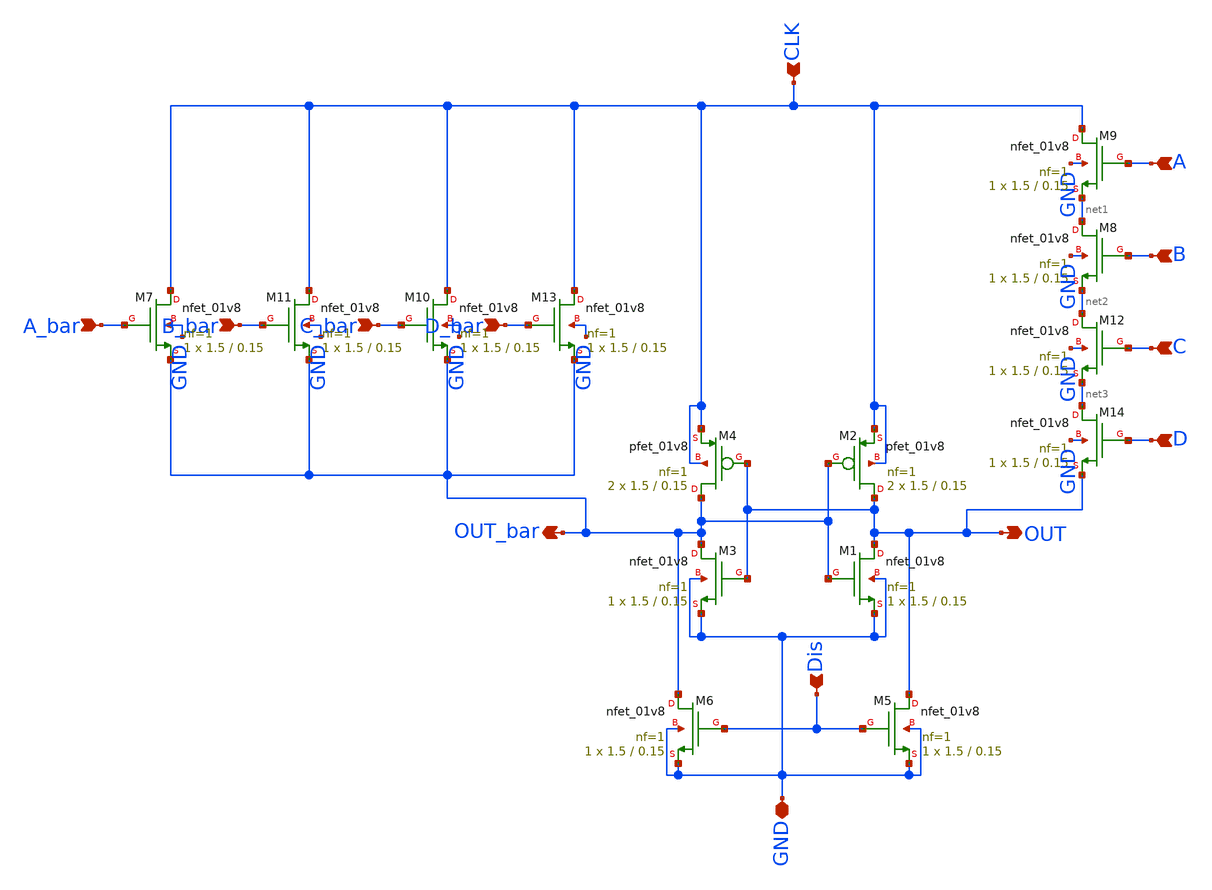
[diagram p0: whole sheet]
** sch_path: skywater_stuff/EESPFAL_4in_NAND.sch
**.subckt EESPFAL_4in_NAND A A_bar B B_bar C C_bar D D_bar OUT OUT_bar Dis GND CLK
*.ipin A
*.ipin A_bar
*.ipin B
*.ipin B_bar
*.ipin C
*.ipin C_bar
*.ipin D
*.ipin D_bar
*.opin OUT
*.opin OUT_bar
*.ipin Dis
*.iopin GND
*.ipin CLK
XM2 OUT OUT_bar CLK CLK sky130_fd_pr__pfet_01v8 L=0.15 W=1.5 nf=1 ad='int((nf+1)/2) * W/nf * 0.29' as='int((nf+2)/2) * W/nf * 0.29'
+ pd='2*int((nf+1)/2) * (W/nf + 0.29)' ps='2*int((nf+2)/2) * (W/nf + 0.29)' nrd='0.29 / W' nrs='0.29 / W'
+ sa=0 sb=0 sd=0 mult=2 m=2
XM11 CLK B_bar OUT_bar GND sky130_fd_pr__nfet_01v8 L=0.15 W=1.5 nf=1 ad='int((nf+1)/2) * W/nf * 0.29'
+ as='int((nf+2)/2) * W/nf * 0.29' pd='2*int((nf+1)/2) * (W/nf + 0.29)' ps='2*int((nf+2)/2) * (W/nf + 0.29)'
+ nrd='0.29 / W' nrs='0.29 / W' sa=0 sb=0 sd=0 mult=1 m=1
XM7 CLK A_bar OUT_bar GND sky130_fd_pr__nfet_01v8 L=0.15 W=1.5 nf=1 ad='int((nf+1)/2) * W/nf * 0.29'
+ as='int((nf+2)/2) * W/nf * 0.29' pd='2*int((nf+1)/2) * (W/nf + 0.29)' ps='2*int((nf+2)/2) * (W/nf + 0.29)'
+ nrd='0.29 / W' nrs='0.29 / W' sa=0 sb=0 sd=0 mult=1 m=1
XM8 net1 B net2 GND sky130_fd_pr__nfet_01v8 L=0.15 W=1.5 nf=1 ad='int((nf+1)/2) * W/nf * 0.29' as='int((nf+2)/2) * W/nf * 0.29'
+ pd='2*int((nf+1)/2) * (W/nf + 0.29)' ps='2*int((nf+2)/2) * (W/nf + 0.29)' nrd='0.29 / W' nrs='0.29 / W'
+ sa=0 sb=0 sd=0 mult=1 m=1
XM1 OUT OUT_bar GND GND sky130_fd_pr__nfet_01v8 L=0.15 W=1.5 nf=1 ad='int((nf+1)/2) * W/nf * 0.29' as='int((nf+2)/2) * W/nf * 0.29'
+ pd='2*int((nf+1)/2) * (W/nf + 0.29)' ps='2*int((nf+2)/2) * (W/nf + 0.29)' nrd='0.29 / W' nrs='0.29 / W'
+ sa=0 sb=0 sd=0 mult=1 m=1
XM5 OUT Dis GND GND sky130_fd_pr__nfet_01v8 L=0.15 W=1.5 nf=1 ad='int((nf+1)/2) * W/nf * 0.29' as='int((nf+2)/2) * W/nf * 0.29'
+ pd='2*int((nf+1)/2) * (W/nf + 0.29)' ps='2*int((nf+2)/2) * (W/nf + 0.29)' nrd='0.29 / W' nrs='0.29 / W'
+ sa=0 sb=0 sd=0 mult=1 m=1
XM6 OUT_bar Dis GND GND sky130_fd_pr__nfet_01v8 L=0.15 W=1.5 nf=1 ad='int((nf+1)/2) * W/nf * 0.29' as='int((nf+2)/2) * W/nf * 0.29'
+ pd='2*int((nf+1)/2) * (W/nf + 0.29)' ps='2*int((nf+2)/2) * (W/nf + 0.29)' nrd='0.29 / W' nrs='0.29 / W'
+ sa=0 sb=0 sd=0 mult=1 m=1
XM10 CLK C_bar OUT_bar GND sky130_fd_pr__nfet_01v8 L=0.15 W=1.5 nf=1 ad='int((nf+1)/2) * W/nf * 0.29'
+ as='int((nf+2)/2) * W/nf * 0.29' pd='2*int((nf+1)/2) * (W/nf + 0.29)' ps='2*int((nf+2)/2) * (W/nf + 0.29)'
+ nrd='0.29 / W' nrs='0.29 / W' sa=0 sb=0 sd=0 mult=1 m=1
XM9 CLK A net1 GND sky130_fd_pr__nfet_01v8 L=0.15 W=1.5 nf=1 ad='int((nf+1)/2) * W/nf * 0.29' as='int((nf+2)/2) * W/nf * 0.29'
+ pd='2*int((nf+1)/2) * (W/nf + 0.29)' ps='2*int((nf+2)/2) * (W/nf + 0.29)' nrd='0.29 / W' nrs='0.29 / W'
+ sa=0 sb=0 sd=0 mult=1 m=1
XM12 net2 C net3 GND sky130_fd_pr__nfet_01v8 L=0.15 W=1.5 nf=1 ad='int((nf+1)/2) * W/nf * 0.29' as='int((nf+2)/2) * W/nf * 0.29'
+ pd='2*int((nf+1)/2) * (W/nf + 0.29)' ps='2*int((nf+2)/2) * (W/nf + 0.29)' nrd='0.29 / W' nrs='0.29 / W'
+ sa=0 sb=0 sd=0 mult=1 m=1
XM4 OUT_bar OUT CLK CLK sky130_fd_pr__pfet_01v8 L=0.15 W=1.5 nf=1 ad='int((nf+1)/2) * W/nf * 0.29' as='int((nf+2)/2) * W/nf * 0.29'
+ pd='2*int((nf+1)/2) * (W/nf + 0.29)' ps='2*int((nf+2)/2) * (W/nf + 0.29)' nrd='0.29 / W' nrs='0.29 / W'
+ sa=0 sb=0 sd=0 mult=2 m=2
XM13 CLK D_bar OUT_bar GND sky130_fd_pr__nfet_01v8 L=0.15 W=1.5 nf=1 ad='int((nf+1)/2) * W/nf * 0.29'
+ as='int((nf+2)/2) * W/nf * 0.29' pd='2*int((nf+1)/2) * (W/nf + 0.29)' ps='2*int((nf+2)/2) * (W/nf + 0.29)'
+ nrd='0.29 / W' nrs='0.29 / W' sa=0 sb=0 sd=0 mult=1 m=1
XM3 OUT_bar OUT GND GND sky130_fd_pr__nfet_01v8 L=0.15 W=1.5 nf=1 ad='int((nf+1)/2) * W/nf * 0.29' as='int((nf+2)/2) * W/nf * 0.29'
+ pd='2*int((nf+1)/2) * (W/nf + 0.29)' ps='2*int((nf+2)/2) * (W/nf + 0.29)' nrd='0.29 / W' nrs='0.29 / W'
+ sa=0 sb=0 sd=0 mult=1 m=1
XM14 net3 D OUT GND sky130_fd_pr__nfet_01v8 L=0.15 W=1.5 nf=1 ad='int((nf+1)/2) * W/nf * 0.29' as='int((nf+2)/2) * W/nf * 0.29'
+ pd='2*int((nf+1)/2) * (W/nf + 0.29)' ps='2*int((nf+2)/2) * (W/nf + 0.29)' nrd='0.29 / W' nrs='0.29 / W'
+ sa=0 sb=0 sd=0 mult=1 m=1
**.ends
.end
